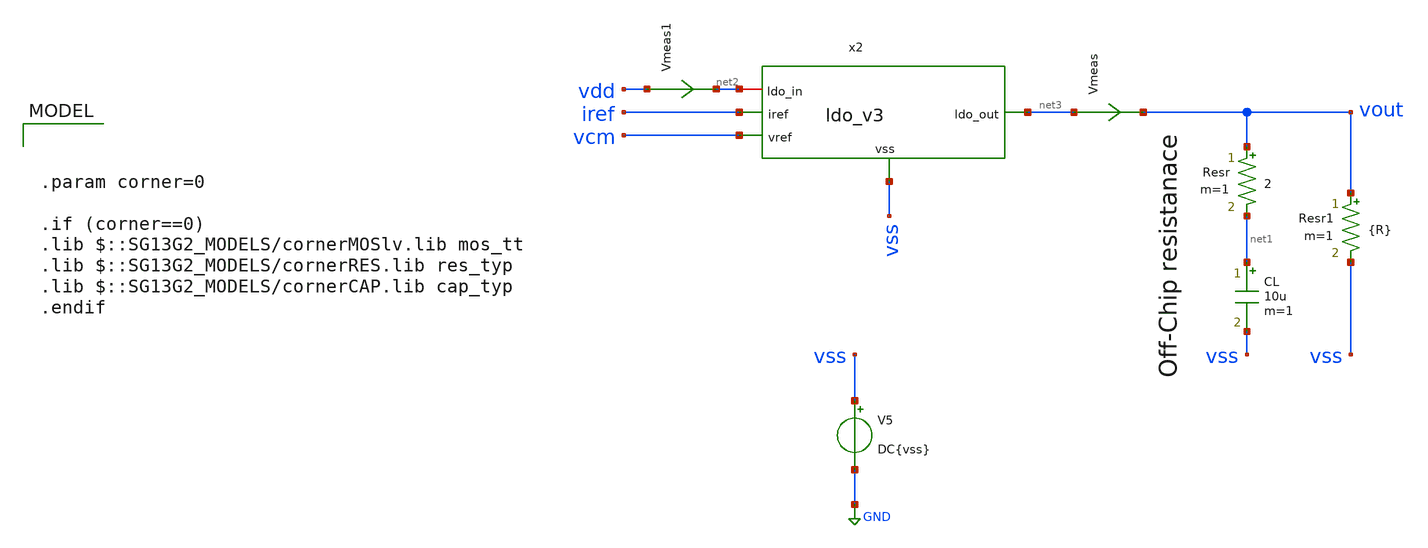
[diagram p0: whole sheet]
** sch_path: v3/m3_ldo_ihp_v3_tb_closeloop.sch
**.subckt m3_ldo_ihp_v3_tb_closeloop
V5 vss GND DC{vss}
Vmeas net3 vout 0
.save i(vmeas)
Vmeas1 vdd net2 0
.save i(vmeas1)
CL net1 vss 10u m=1
Resr vout net1 2 m=1
x2 net2 net3 iref vcm vss ldo_v3
Resr1 vout vss {R} m=1
**** begin user architecture code


.param corner=0

.if (corner==0)
.lib $::SG13G2_MODELS/cornerMOSlv.lib mos_tt
.lib $::SG13G2_MODELS/cornerRES.lib res_typ
.lib $::SG13G2_MODELS/cornerCAP.lib cap_typ
.endif




Vs vdd 0 1.8 AC 1
Vref vcm 0 0.9
Iin iref 0 5e-6

.param temp=27
.save all






.param R=18
*R10 vout 0 {R}
IL vout 0 PWL(0 0.1m 10u 0.1m 20u 10m 30u 10m)
*CL vout 0 50p






.param vdd  = 1.8
.param vss  = 0.0
.param vac  = 60m

.param w857 = 6u
.param l857 = 2u

.param wpar = 15u
.param lpar = 2u
.param mpar = 1

.param w34  = 2u
.param l34  = 1u
.param m34  = 1

.param w6   = 20u
.param l6   = 0.5u
.param m6   = 1

.param w7   = w857*4
.param w5   = w857*1





.param mm_ok=1
.param mc_ok=1
.param temp=27

.control
pre_osdi /home/ac3e/Documents/psp103_nqs.osdi

define gauss ( nom , var , sig ) ( nom + nom * var / sig * sgauss (0))

let mc_runs = 10
let run = 0
set curplot=new
set scratch=$curplot
setplot $scratch
let vout=unitvec(mc_runs)
let vdd=unitvec(mc_runs)
let vcm=unitvec(mc_runs)
let iref=unitvec(mc_runs)

***************** LOOP *********************
dowhile run < mc_runs
alter vs = gauss (1.8 , 0.2 , 3)
alter vref = gauss (0.9 , 0.01 , 3)
alter iin = gauss (5e-6 , 0.1e-6 , 3)
*dc Vds 0 3 0.01
op
set run=$&run
set dt=$curplot
setplot $scratch
let out{$run}={$dt}.v(vout)
let Vout[run]={$dt}.v(vout)
let Vdd[run]={$dt}.v(vdd)
let Vcm[run]={$dt}.v(vcm)
let Iref[run]={$dt}.i(Iref)
setplot $dt
reset
let run=run+1
end
***************** LOOP *********************

plot {$scratch}.all

wrdata /home/ac3e/Documents/ihp_design/v3/mc_ldo_closeloop.csv {$scratch}.vout {$scratch}.vdd {$scratch}.vcm
+ {$scratch}.iref
write /home/ac3e/Documents/ihp_design/v3/mc_ldo_closeloop.raw
echo
print {$scratch}.vout {$scratch}.vdd {$scratch}.vcm {$scratch}.iref

.endc


**** end user architecture code
**.ends
.GLOBAL GND
.end
